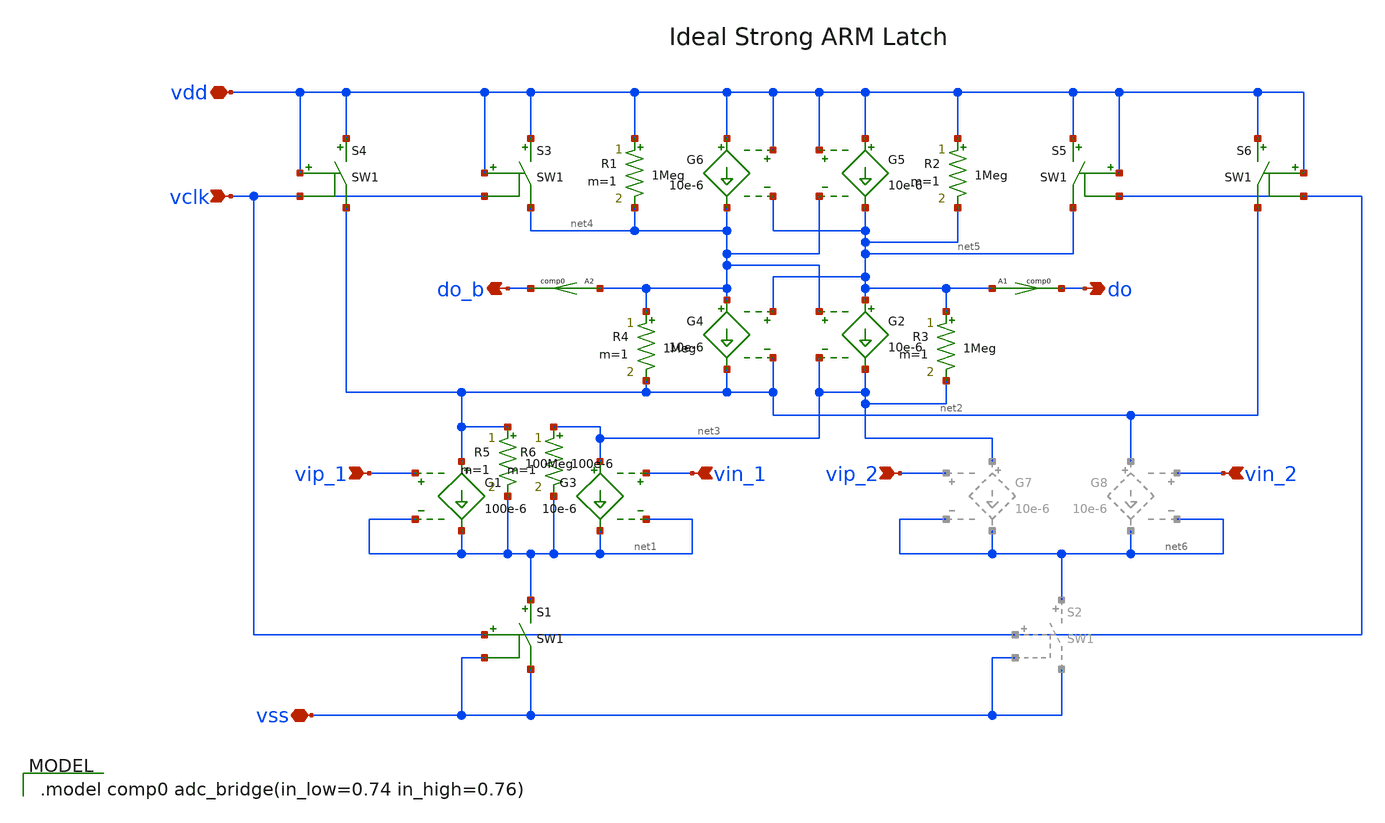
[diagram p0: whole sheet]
** sch_path: xschem/sal-macro.sch
**.subckt sal-macro vss vip_1 vip_2 vin_2 do vin_1 vdd do_b vclk
*.iopin vss
*.ipin vip_1
*.ipin vip_2
*.ipin vin_2
*.opin do
*.ipin vin_1
*.iopin vdd
*.opin do_b
*.ipin vclk
A1 [ net5 ] [ do ] comp0
G1 net2 net1 vip_1 net1 100e-6
G3 net3 net1 vin_1 net1 10e-6
S1 net1 vss vclk vss SW1
G2 net5 net3 net4 net3 10e-6
G4 net4 net2 net5 net2 10e-6
G5 vdd net5 vdd net4 10e-6
G6 vdd net4 vdd net5 10e-6
S3 vdd net4 vdd vclk SW1
S4 vdd net2 vdd vclk SW1
S5 vdd net5 vdd vclk SW1
S6 vdd net2 vdd vclk SW1
A2 [ net4 ] [ do_b ] comp0
R1 vdd net4 1Meg m=1
R2 vdd net5 1Meg m=1
R3 net5 net3 1Meg m=1
R4 net4 net2 1Meg m=1
R5 net2 net1 100Meg m=1
R6 net3 net1 100e-6 m=1
**.ends
**** begin user architecture code

.model comp0 adc_bridge(in_low=0.74 in_high=0.76)

.MODEL SW1 SW( VT=0.75 VH=0.01 RON=1 ROFF=100Meg )
**** end user architecture code
.end
